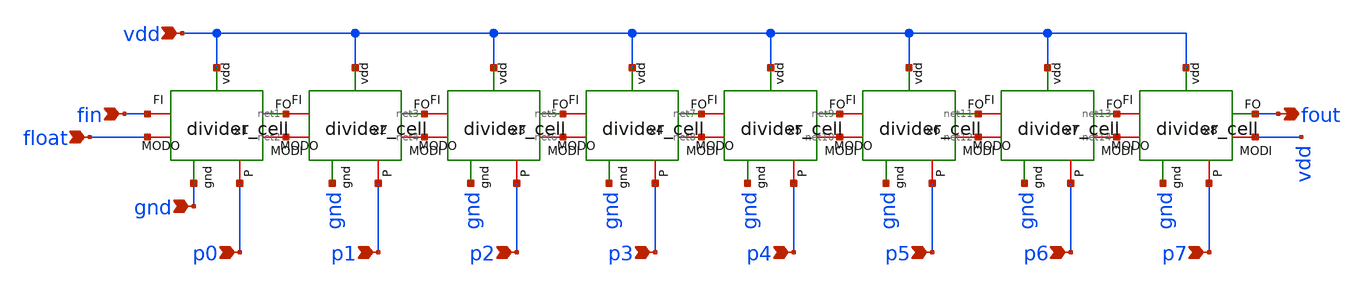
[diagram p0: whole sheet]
** sch_path: pll/dividers_lib/divider/xschem/divider.sch
**.subckt divider vdd fin gnd fout p0 p1 p2 p3 p4 p5 p6 p7 float
*.ipin vdd
*.ipin fin
*.ipin gnd
*.opin fout
*.ipin p0
*.ipin p1
*.ipin p2
*.ipin p3
*.ipin p4
*.ipin p5
*.ipin p6
*.ipin p7
*.ipin float
x1 vdd net1 fin p0 float gnd net2 divider_cell
x2 vdd net3 net1 p1 net2 gnd net4 divider_cell
x3 vdd net5 net3 p2 net4 gnd net6 divider_cell
x4 vdd net7 net5 p3 net6 gnd net8 divider_cell
x5 vdd net9 net7 p4 net8 gnd net10 divider_cell
x6 vdd net11 net9 p5 net10 gnd net12 divider_cell
x7 vdd net13 net11 p6 net12 gnd net14 divider_cell
x8 vdd fout net13 p7 net14 gnd vdd divider_cell
**.ends
.end
